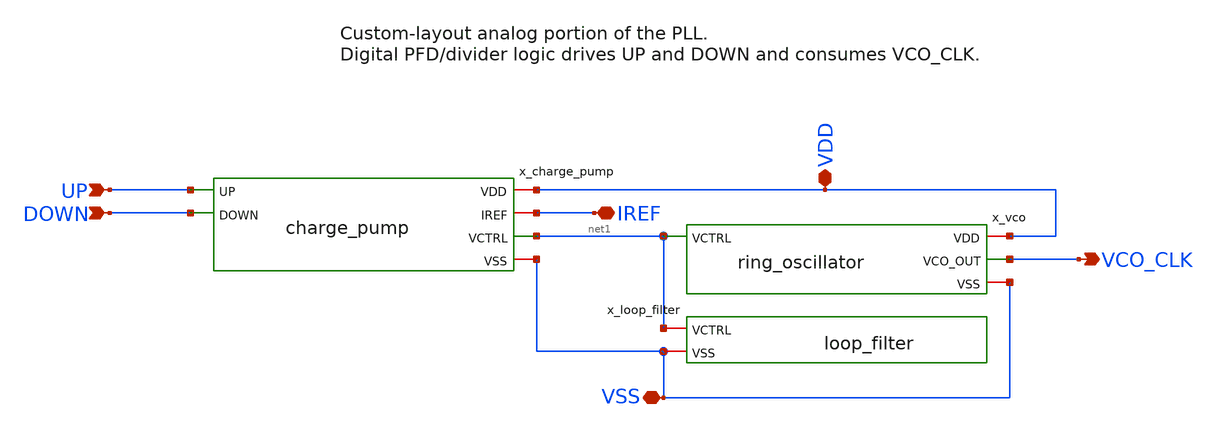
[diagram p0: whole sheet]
** sch_path: macros/pll_analog/schematic/xschem/pll_analog.sch
**.subckt pll_analog UP DOWN IREF VCO_CLK VDD VSS
*.ipin UP
*.ipin DOWN
*.iopin IREF
*.opin VCO_CLK
*.iopin VDD
*.iopin VSS
x_charge_pump VDD UP DOWN IREF net1 VSS charge_pump
x_loop_filter net1 VSS loop_filter
x_vco VDD VCO_CLK net1 VSS ring_oscillator
**.ends
.end
